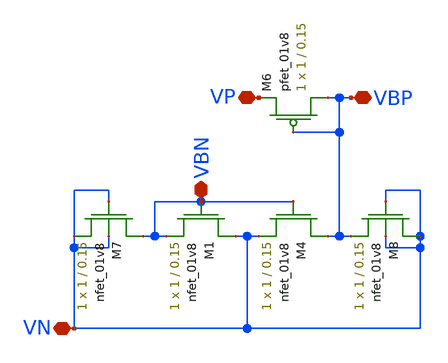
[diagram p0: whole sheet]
** sch_path: schematic/bias_gen_lds.sch
**.subckt bias_gen_lds VN VP VBP VBN
*.iopin VN
*.iopin VP
*.iopin VBP
*.iopin VBN
XM4 VBP VBN VN VN sky130_fd_pr__nfet_01v8 L=0.15 W=1 nf=1 ad='int((nf+1)/2) * W/nf * 0.29' as='int((nf+2)/2) * W/nf * 0.29'
+ pd='2*int((nf+1)/2) * (W/nf + 0.29)' ps='2*int((nf+2)/2) * (W/nf + 0.29)' nrd='0.29 / W' nrs='0.29 / W'
+ sa=0 sb=0 sd=0 mult=1 m=1
XM6 VBP VBP VP VP sky130_fd_pr__pfet_01v8 L=0.15 W=1 nf=1 ad='int((nf+1)/2) * W/nf * 0.29' as='int((nf+2)/2) * W/nf * 0.29'
+ pd='2*int((nf+1)/2) * (W/nf + 0.29)' ps='2*int((nf+2)/2) * (W/nf + 0.29)' nrd='0.29 / W' nrs='0.29 / W'
+ sa=0 sb=0 sd=0 mult=1 m=1
XM7 VBN VN VN VN sky130_fd_pr__nfet_01v8 L=0.15 W=1 nf=1 ad='int((nf+1)/2) * W/nf * 0.29' as='int((nf+2)/2) * W/nf * 0.29'
+ pd='2*int((nf+1)/2) * (W/nf + 0.29)' ps='2*int((nf+2)/2) * (W/nf + 0.29)' nrd='0.29 / W' nrs='0.29 / W'
+ sa=0 sb=0 sd=0 mult=1 m=1
XM8 VN VN VBP VN sky130_fd_pr__nfet_01v8 L=0.15 W=1 nf=1 ad='int((nf+1)/2) * W/nf * 0.29' as='int((nf+2)/2) * W/nf * 0.29'
+ pd='2*int((nf+1)/2) * (W/nf + 0.29)' ps='2*int((nf+2)/2) * (W/nf + 0.29)' nrd='0.29 / W' nrs='0.29 / W'
+ sa=0 sb=0 sd=0 mult=1 m=1
XM1 VN VBN VBN VN sky130_fd_pr__nfet_01v8 L=0.15 W=1 nf=1 ad='int((nf+1)/2) * W/nf * 0.29' as='int((nf+2)/2) * W/nf * 0.29'
+ pd='2*int((nf+1)/2) * (W/nf + 0.29)' ps='2*int((nf+2)/2) * (W/nf + 0.29)' nrd='0.29 / W' nrs='0.29 / W'
+ sa=0 sb=0 sd=0 mult=1 m=1
**.ends
.end
